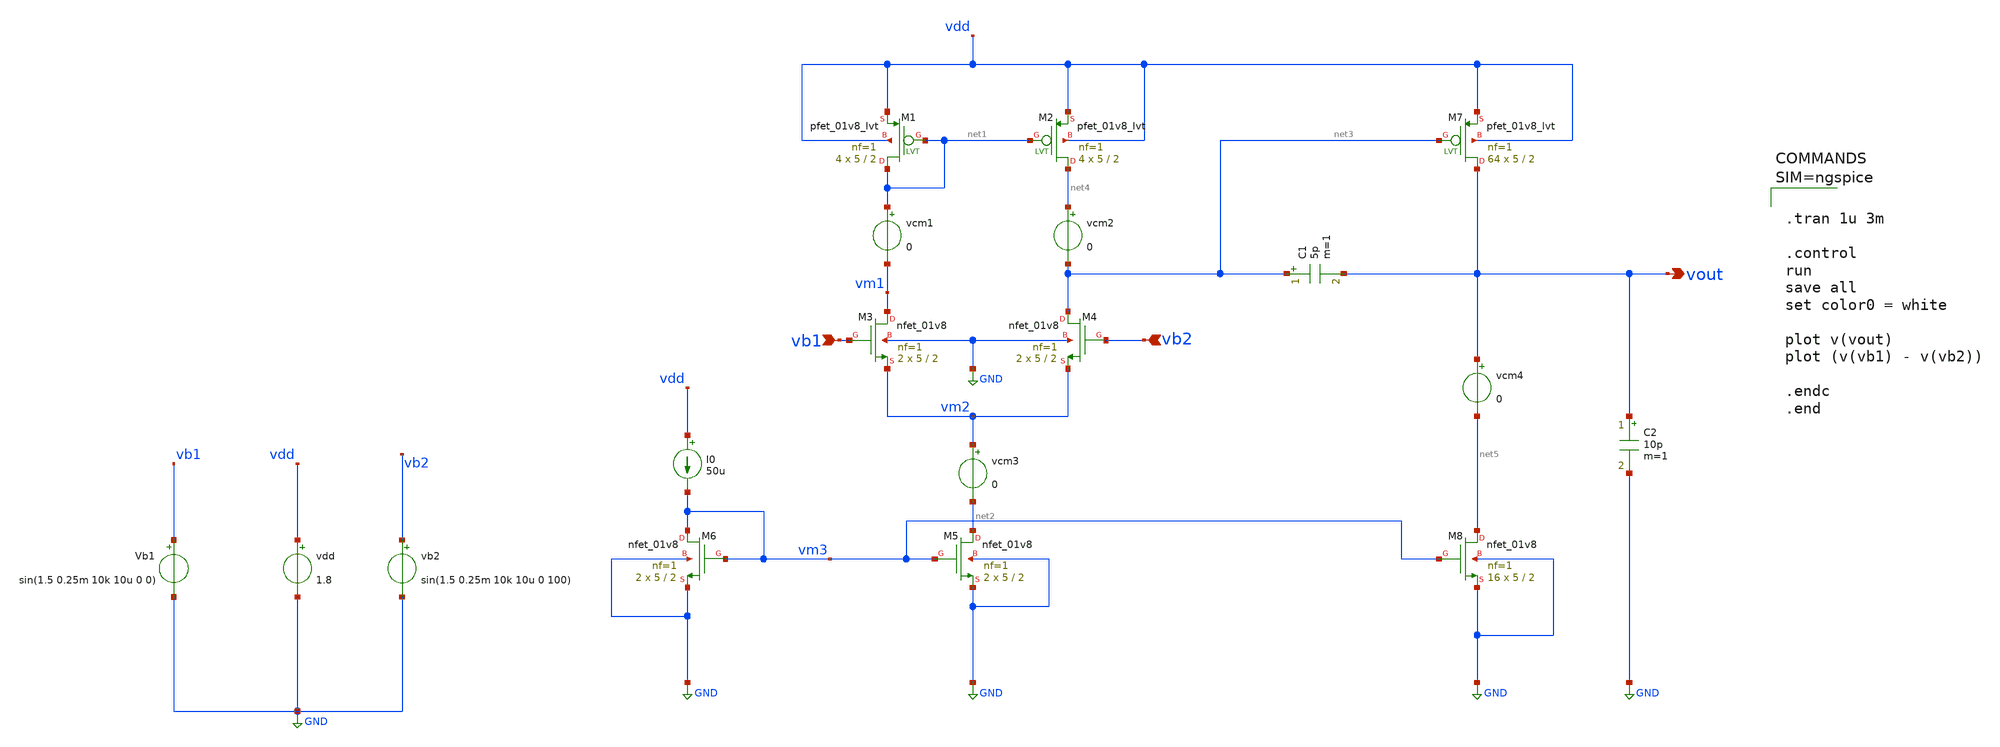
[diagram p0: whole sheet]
** sch_path: sch/Differential_Amplifier_AC_transient_Sine_Waves.sch
**.subckt Differential_Amplifier_AC_transient_Sine_Waves vout vb2 vb1
*.opin vout
*.ipin vb2
*.ipin vb1
XM5 net2 vm3 GND GND sky130_fd_pr__nfet_01v8 L=2 W=5 nf=1 ad='int((1 + 1)/2) * 5 / 1 * 0.29' as='int((1 + 2)/2) * 5 / 1 * 0.29'
+ pd='2*int((1 + 1)/2) * (5 / 1 + 0.29)' ps='2*int((1 + 2)/2) * (5 / 1 + 0.29)' nrd='0.29 / 5 ' nrs='0.29 / 5 '
+ sa=0 sb=0 sd=0 mult=2 m=2
I0 vdd vm3 50u
XM2 net4 net1 vdd vdd sky130_fd_pr__pfet_01v8_lvt L=2 W=5 nf=1 ad='int((1 + 1)/2) * 5 / 1 * 0.29' as='int((1 + 2)/2) * 5 / 1 * 0.29'
+ pd='2*int((1 + 1)/2) * (5 / 1 + 0.29)' ps='2*int((1 + 2)/2) * (5 / 1 + 0.29)' nrd='0.29 / 5 ' nrs='0.29 / 5 '
+ sa=0 sb=0 sd=0 mult=4 m=4
XM3 vm1 vb1 vm2 GND sky130_fd_pr__nfet_01v8 L=2 W=5 nf=1 ad='int((1 + 1)/2) * 5 / 1 * 0.29' as='int((1 + 2)/2) * 5 / 1 * 0.29'
+ pd='2*int((1 + 1)/2) * (5 / 1 + 0.29)' ps='2*int((1 + 2)/2) * (5 / 1 + 0.29)' nrd='0.29 / 5 ' nrs='0.29 / 5 '
+ sa=0 sb=0 sd=0 mult=2 m=2
XM4 net3 vb2 vm2 GND sky130_fd_pr__nfet_01v8 L=2 W=5 nf=1 ad='int((1 + 1)/2) * 5 / 1 * 0.29' as='int((1 + 2)/2) * 5 / 1 * 0.29'
+ pd='2*int((1 + 1)/2) * (5 / 1 + 0.29)' ps='2*int((1 + 2)/2) * (5 / 1 + 0.29)' nrd='0.29 / 5 ' nrs='0.29 / 5 '
+ sa=0 sb=0 sd=0 mult=2 m=2
XM6 vm3 vm3 GND GND sky130_fd_pr__nfet_01v8 L=2 W=5 nf=1 ad='int((1 + 1)/2) * 5 / 1 * 0.29' as='int((1 + 2)/2) * 5 / 1 * 0.29'
+ pd='2*int((1 + 1)/2) * (5 / 1 + 0.29)' ps='2*int((1 + 2)/2) * (5 / 1 + 0.29)' nrd='0.29 / 5 ' nrs='0.29 / 5 '
+ sa=0 sb=0 sd=0 mult=2 m=2
XM1 net1 net1 vdd vdd sky130_fd_pr__pfet_01v8_lvt L=2 W=5 nf=1 ad='int((1 + 1)/2) * 5 / 1 * 0.29' as='int((1 + 2)/2) * 5 / 1 * 0.29'
+ pd='2*int((1 + 1)/2) * (5 / 1 + 0.29)' ps='2*int((1 + 2)/2) * (5 / 1 + 0.29)' nrd='0.29 / 5 ' nrs='0.29 / 5 '
+ sa=0 sb=0 sd=0 mult=4 m=4
vcm3 vm2 net2 0
vcm1 net1 vm1 0
vcm2 net4 net3 0
XM7 vout net3 vdd vdd sky130_fd_pr__pfet_01v8_lvt L=2 W=5 nf=1 ad='int((1 + 1)/2) * 5 / 1 * 0.29' as='int((1 + 2)/2) * 5 / 1 * 0.29'
+ pd='2*int((1 + 1)/2) * (5 / 1 + 0.29)' ps='2*int((1 + 2)/2) * (5 / 1 + 0.29)' nrd='0.29 / 5 ' nrs='0.29 / 5 '
+ sa=0 sb=0 sd=0 mult=64 m=64
XM8 net5 vm3 GND GND sky130_fd_pr__nfet_01v8 L=2 W=5 nf=1 ad='int((1 + 1)/2) * 5 / 1 * 0.29' as='int((1 + 2)/2) * 5 / 1 * 0.29'
+ pd='2*int((1 + 1)/2) * (5 / 1 + 0.29)' ps='2*int((1 + 2)/2) * (5 / 1 + 0.29)' nrd='0.29 / 5 ' nrs='0.29 / 5 '
+ sa=0 sb=0 sd=0 mult=16 m=16
C1 net3 vout 5p m=1
vcm4 vout net5 0
C2 vout GND 10p m=1
vdd vdd GND 1.8
Vb1 vb1 GND sin(1.5 0.25m 10k 10u 0 0)
vb2 vb2 GND sin(1.5 0.25m 10k 10u 0 100)
**** begin user architecture code

** opencircuitdesign pdks install
.lib $::SKYWATER_MODELS/sky130.lib.spice tt




.tran 1u 3m

.control
run
save all
set color0 = white

plot v(vout)
plot (v(vb1) - v(vb2))

.endc
.end




**** end user architecture code
**.ends
.GLOBAL GND
.end
